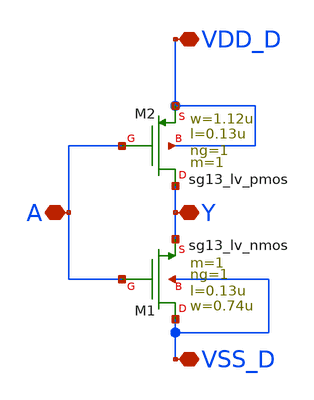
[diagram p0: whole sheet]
** sch_path: Day1/inv_1_manual.sch
**.subckt inv_1_manual VDD_D VSS_D A Y
*.iopin VDD_D
*.iopin VSS_D
*.iopin A
*.iopin Y
XM1 VSS_D A Y VSS_D sg13_lv_nmos w=0.74u l=0.13u ng=1 m=1 mm_ok=1
XM2 Y A VDD_D VDD_D sg13_lv_pmos w=1.12u l=0.13u ng=1 m=1 mm_ok=1
**.ends
.end
